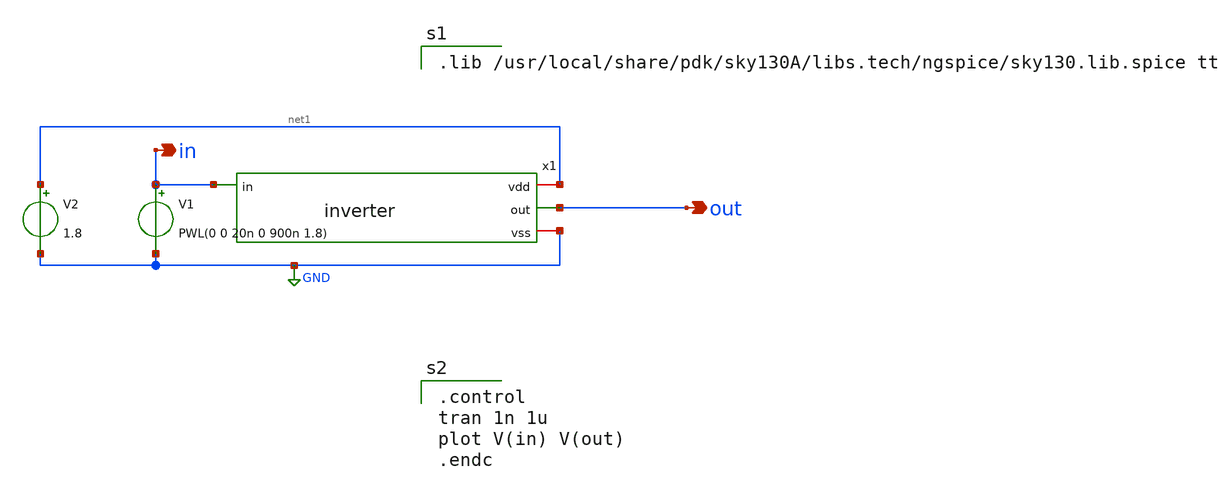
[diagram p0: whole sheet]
** sch_path: Lab1_inverter/xschem/inverter_tb.sch
**.subckt inverter_tb out in
*.opin out
*.opin in
x1 net1 in out GND inverter
V1 in GND PWL(0 0 20n 0 900n 1.8)
V2 net1 GND 1.8
**** begin user architecture code

.control
tran 1n 1u
plot V(in) V(out)
.endc


.lib /usr/local/share/pdk/sky130A/libs.tech/ngspice/sky130.lib.spice tt

**** end user architecture code
**.ends

* expanding   symbol:  inverter.sym # of pins=4
** sym_path: Lab1_inverter/xschem/inverter.sym
** sch_path: Lab1_inverter/xschem/inverter.sch
.subckt inverter vdd in out vss
*.ipin in
*.opin out
*.iopin vdd
*.iopin vss
XM1 out in vss vss sky130_fd_pr__nfet_01v8 L=0.18 W=4.5 nf=3 ad='int((nf + 1)/2) * W / nf * 0.29' as='int((nf + 2)/2) * W / nf * 0.29'
+ pd='2*int((nf + 1)/2) * (W / nf + 0.29)' ps='2*int((nf + 2)/2) * (W / nf + 0.29)' nrd='0.29 / W ' nrs='0.29 / W '
+ sa=0 sb=0 sd=0 mult=1 m=1
XM2 out in vdd vdd sky130_fd_pr__pfet_01v8 L=0.18 W=3 nf=3 ad='int((nf + 1)/2) * W / nf * 0.29' as='int((nf + 2)/2) * W / nf * 0.29'
+ pd='2*int((nf + 1)/2) * (W / nf + 0.29)' ps='2*int((nf + 2)/2) * (W / nf + 0.29)' nrd='0.29 / W ' nrs='0.29 / W '
+ sa=0 sb=0 sd=0 mult=1 m=1
.ends

.GLOBAL GND
.end
